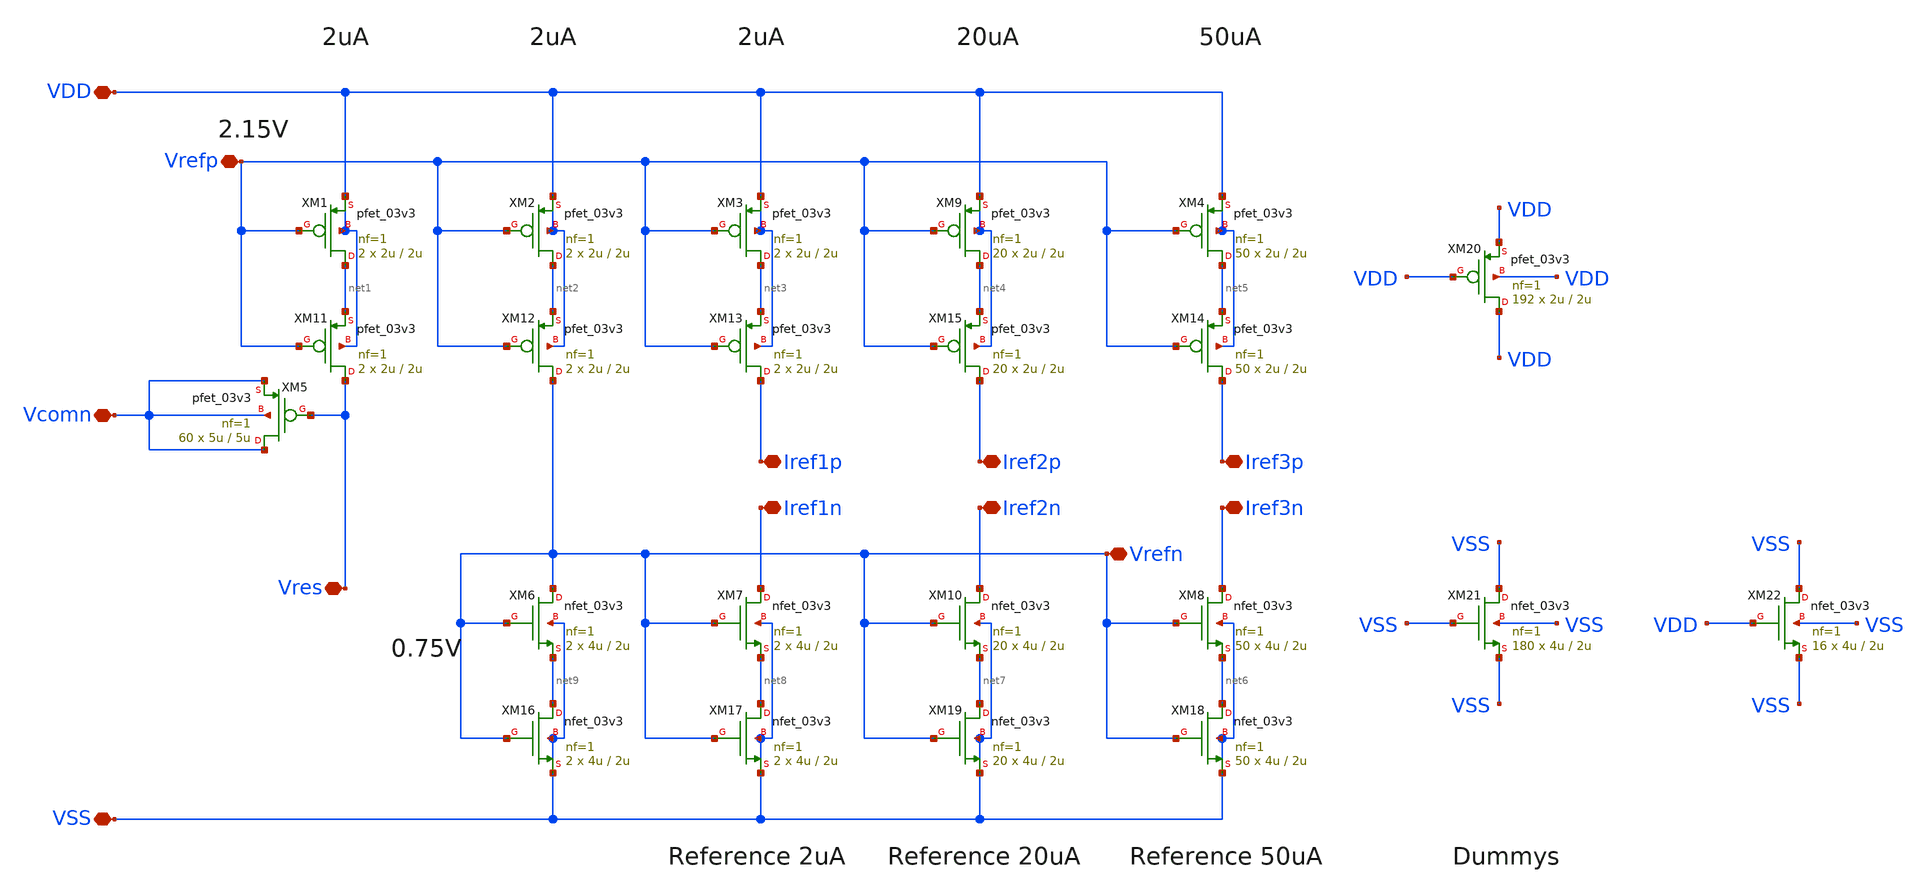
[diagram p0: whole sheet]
** sch_path: designs/libs/current_reference_second_stage_v2/xschem/current_reference_second_stage_v2.sch
**.subckt current_reference_second_stage_v2 VDD VSS Vrefp Vrefn Iref1n Iref3n Iref1p Iref3p Vres
*+ Vcomn Iref2p Iref2n
*.iopin VDD
*.iopin VSS
*.iopin Vrefp
*.iopin Vrefn
*.iopin Iref1n
*.iopin Iref3n
*.iopin Iref1p
*.iopin Iref3p
*.iopin Vres
*.iopin Vcomn
*.iopin Iref2p
*.iopin Iref2n
XM6 Vrefn Vrefn net9 VSS nfet_03v3 L=2u W=4u nf=1 ad='int((nf+1)/2) * W/nf * 0.18u' as='int((nf+2)/2) * W/nf * 0.18u'
+ pd='2*int((nf+1)/2) * (W/nf + 0.18u)' ps='2*int((nf+2)/2) * (W/nf + 0.18u)' nrd='0.18u / W' nrs='0.18u / W'
+ sa=0 sb=0 sd=0 m=2
XM5 Vcomn Vres Vcomn Vcomn pfet_03v3 L=5u W=5u nf=1 ad='int((nf+1)/2) * W/nf * 0.18u' as='int((nf+2)/2) * W/nf * 0.18u'
+ pd='2*int((nf+1)/2) * (W/nf + 0.18u)' ps='2*int((nf+2)/2) * (W/nf + 0.18u)' nrd='0.18u / W' nrs='0.18u / W'
+ sa=0 sb=0 sd=0 m=60
XM1 net1 Vrefp VDD VDD pfet_03v3 L=2u W=2u nf=1 ad='int((nf+1)/2) * W/nf * 0.18u' as='int((nf+2)/2) * W/nf * 0.18u'
+ pd='2*int((nf+1)/2) * (W/nf + 0.18u)' ps='2*int((nf+2)/2) * (W/nf + 0.18u)' nrd='0.18u / W' nrs='0.18u / W'
+ sa=0 sb=0 sd=0 m=2
XM2 net2 Vrefp VDD VDD pfet_03v3 L=2u W=2u nf=1 ad='int((nf+1)/2) * W/nf * 0.18u' as='int((nf+2)/2) * W/nf * 0.18u'
+ pd='2*int((nf+1)/2) * (W/nf + 0.18u)' ps='2*int((nf+2)/2) * (W/nf + 0.18u)' nrd='0.18u / W' nrs='0.18u / W'
+ sa=0 sb=0 sd=0 m=2
XM3 net3 Vrefp VDD VDD pfet_03v3 L=2u W=2u nf=1 ad='int((nf+1)/2) * W/nf * 0.18u' as='int((nf+2)/2) * W/nf * 0.18u'
+ pd='2*int((nf+1)/2) * (W/nf + 0.18u)' ps='2*int((nf+2)/2) * (W/nf + 0.18u)' nrd='0.18u / W' nrs='0.18u / W'
+ sa=0 sb=0 sd=0 m=2
XM4 net5 Vrefp VDD VDD pfet_03v3 L=2u W=2u nf=1 ad='int((nf+1)/2) * W/nf * 0.18u' as='int((nf+2)/2) * W/nf * 0.18u'
+ pd='2*int((nf+1)/2) * (W/nf + 0.18u)' ps='2*int((nf+2)/2) * (W/nf + 0.18u)' nrd='0.18u / W' nrs='0.18u / W'
+ sa=0 sb=0 sd=0 m=50
XM7 Iref1n Vrefn net8 VSS nfet_03v3 L=2u W=4u nf=1 ad='int((nf+1)/2) * W/nf * 0.18u' as='int((nf+2)/2) * W/nf * 0.18u'
+ pd='2*int((nf+1)/2) * (W/nf + 0.18u)' ps='2*int((nf+2)/2) * (W/nf + 0.18u)' nrd='0.18u / W' nrs='0.18u / W'
+ sa=0 sb=0 sd=0 m=2
XM8 Iref3n Vrefn net6 VSS nfet_03v3 L=2u W=4u nf=1 ad='int((nf+1)/2) * W/nf * 0.18u' as='int((nf+2)/2) * W/nf * 0.18u'
+ pd='2*int((nf+1)/2) * (W/nf + 0.18u)' ps='2*int((nf+2)/2) * (W/nf + 0.18u)' nrd='0.18u / W' nrs='0.18u / W'
+ sa=0 sb=0 sd=0 m=50
XM9 net4 Vrefp VDD VDD pfet_03v3 L=2u W=2u nf=1 ad='int((nf+1)/2) * W/nf * 0.18u' as='int((nf+2)/2) * W/nf * 0.18u'
+ pd='2*int((nf+1)/2) * (W/nf + 0.18u)' ps='2*int((nf+2)/2) * (W/nf + 0.18u)' nrd='0.18u / W' nrs='0.18u / W'
+ sa=0 sb=0 sd=0 m=20
XM10 Iref2n Vrefn net7 VSS nfet_03v3 L=2u W=4u nf=1 ad='int((nf+1)/2) * W/nf * 0.18u' as='int((nf+2)/2) * W/nf * 0.18u'
+ pd='2*int((nf+1)/2) * (W/nf + 0.18u)' ps='2*int((nf+2)/2) * (W/nf + 0.18u)' nrd='0.18u / W' nrs='0.18u / W'
+ sa=0 sb=0 sd=0 m=20
XM11 Vres Vrefp net1 VDD pfet_03v3 L=2u W=2u nf=1 ad='int((nf+1)/2) * W/nf * 0.18u' as='int((nf+2)/2) * W/nf * 0.18u'
+ pd='2*int((nf+1)/2) * (W/nf + 0.18u)' ps='2*int((nf+2)/2) * (W/nf + 0.18u)' nrd='0.18u / W' nrs='0.18u / W'
+ sa=0 sb=0 sd=0 m=2
XM12 Vrefn Vrefp net2 VDD pfet_03v3 L=2u W=2u nf=1 ad='int((nf+1)/2) * W/nf * 0.18u' as='int((nf+2)/2) * W/nf * 0.18u'
+ pd='2*int((nf+1)/2) * (W/nf + 0.18u)' ps='2*int((nf+2)/2) * (W/nf + 0.18u)' nrd='0.18u / W' nrs='0.18u / W'
+ sa=0 sb=0 sd=0 m=2
XM13 Iref1p Vrefp net3 VDD pfet_03v3 L=2u W=2u nf=1 ad='int((nf+1)/2) * W/nf * 0.18u' as='int((nf+2)/2) * W/nf * 0.18u'
+ pd='2*int((nf+1)/2) * (W/nf + 0.18u)' ps='2*int((nf+2)/2) * (W/nf + 0.18u)' nrd='0.18u / W' nrs='0.18u / W'
+ sa=0 sb=0 sd=0 m=2
XM14 Iref3p Vrefp net5 VDD pfet_03v3 L=2u W=2u nf=1 ad='int((nf+1)/2) * W/nf * 0.18u' as='int((nf+2)/2) * W/nf * 0.18u'
+ pd='2*int((nf+1)/2) * (W/nf + 0.18u)' ps='2*int((nf+2)/2) * (W/nf + 0.18u)' nrd='0.18u / W' nrs='0.18u / W'
+ sa=0 sb=0 sd=0 m=50
XM15 Iref2p Vrefp net4 VDD pfet_03v3 L=2u W=2u nf=1 ad='int((nf+1)/2) * W/nf * 0.18u' as='int((nf+2)/2) * W/nf * 0.18u'
+ pd='2*int((nf+1)/2) * (W/nf + 0.18u)' ps='2*int((nf+2)/2) * (W/nf + 0.18u)' nrd='0.18u / W' nrs='0.18u / W'
+ sa=0 sb=0 sd=0 m=20
XM16 net9 Vrefn VSS VSS nfet_03v3 L=2u W=4u nf=1 ad='int((nf+1)/2) * W/nf * 0.18u' as='int((nf+2)/2) * W/nf * 0.18u'
+ pd='2*int((nf+1)/2) * (W/nf + 0.18u)' ps='2*int((nf+2)/2) * (W/nf + 0.18u)' nrd='0.18u / W' nrs='0.18u / W'
+ sa=0 sb=0 sd=0 m=2
XM17 net8 Vrefn VSS VSS nfet_03v3 L=2u W=4u nf=1 ad='int((nf+1)/2) * W/nf * 0.18u' as='int((nf+2)/2) * W/nf * 0.18u'
+ pd='2*int((nf+1)/2) * (W/nf + 0.18u)' ps='2*int((nf+2)/2) * (W/nf + 0.18u)' nrd='0.18u / W' nrs='0.18u / W'
+ sa=0 sb=0 sd=0 m=2
XM18 net6 Vrefn VSS VSS nfet_03v3 L=2u W=4u nf=1 ad='int((nf+1)/2) * W/nf * 0.18u' as='int((nf+2)/2) * W/nf * 0.18u'
+ pd='2*int((nf+1)/2) * (W/nf + 0.18u)' ps='2*int((nf+2)/2) * (W/nf + 0.18u)' nrd='0.18u / W' nrs='0.18u / W'
+ sa=0 sb=0 sd=0 m=50
XM19 net7 Vrefn VSS VSS nfet_03v3 L=2u W=4u nf=1 ad='int((nf+1)/2) * W/nf * 0.18u' as='int((nf+2)/2) * W/nf * 0.18u'
+ pd='2*int((nf+1)/2) * (W/nf + 0.18u)' ps='2*int((nf+2)/2) * (W/nf + 0.18u)' nrd='0.18u / W' nrs='0.18u / W'
+ sa=0 sb=0 sd=0 m=20
XM20 VDD VDD VDD VDD pfet_03v3 L=2u W=2u nf=1 ad='int((nf+1)/2) * W/nf * 0.18u' as='int((nf+2)/2) * W/nf * 0.18u'
+ pd='2*int((nf+1)/2) * (W/nf + 0.18u)' ps='2*int((nf+2)/2) * (W/nf + 0.18u)' nrd='0.18u / W' nrs='0.18u / W'
+ sa=0 sb=0 sd=0 m=192
XM21 VSS VSS VSS VSS nfet_03v3 L=2u W=4u nf=1 ad='int((nf+1)/2) * W/nf * 0.18u' as='int((nf+2)/2) * W/nf * 0.18u'
+ pd='2*int((nf+1)/2) * (W/nf + 0.18u)' ps='2*int((nf+2)/2) * (W/nf + 0.18u)' nrd='0.18u / W' nrs='0.18u / W'
+ sa=0 sb=0 sd=0 m=180
XM22 VSS VDD VSS VSS nfet_03v3 L=2u W=4u nf=1 ad='int((nf+1)/2) * W/nf * 0.18u' as='int((nf+2)/2) * W/nf * 0.18u'
+ pd='2*int((nf+1)/2) * (W/nf + 0.18u)' ps='2*int((nf+2)/2) * (W/nf + 0.18u)' nrd='0.18u / W' nrs='0.18u / W'
+ sa=0 sb=0 sd=0 m=16
**.ends
.end
